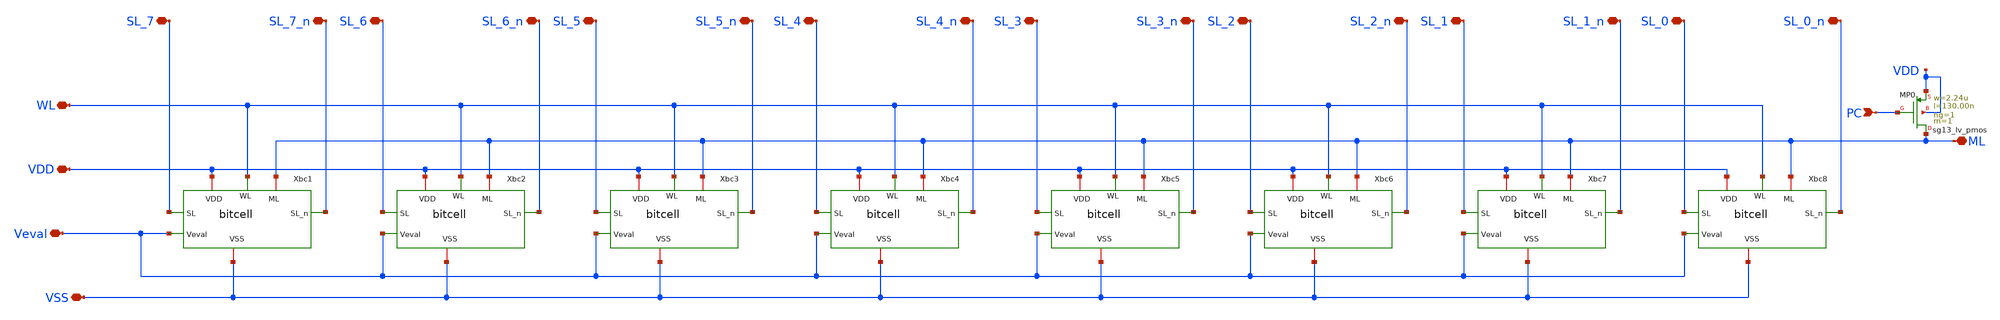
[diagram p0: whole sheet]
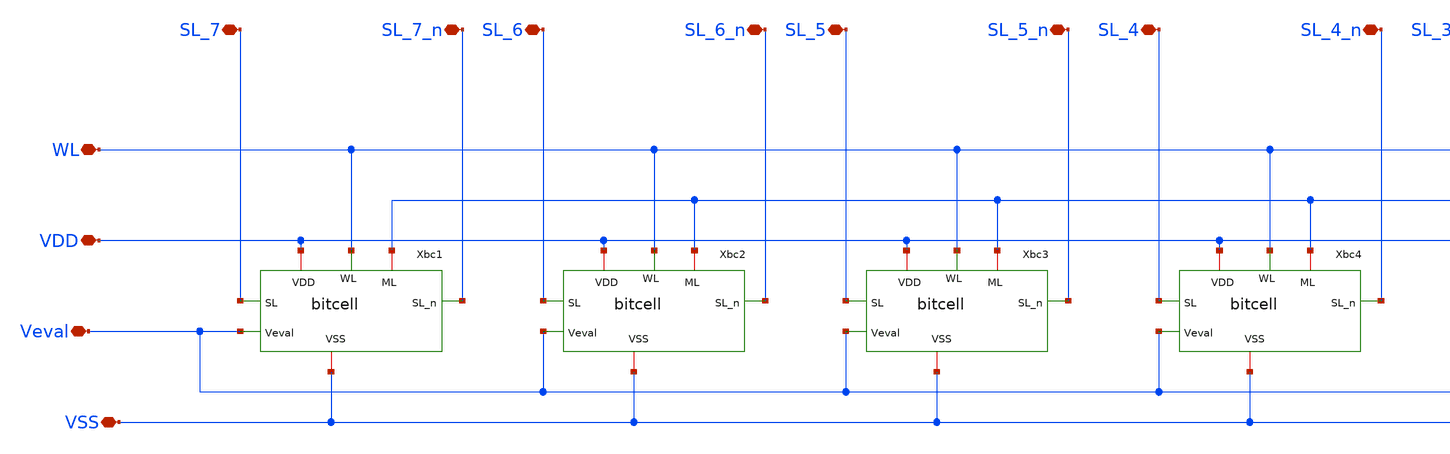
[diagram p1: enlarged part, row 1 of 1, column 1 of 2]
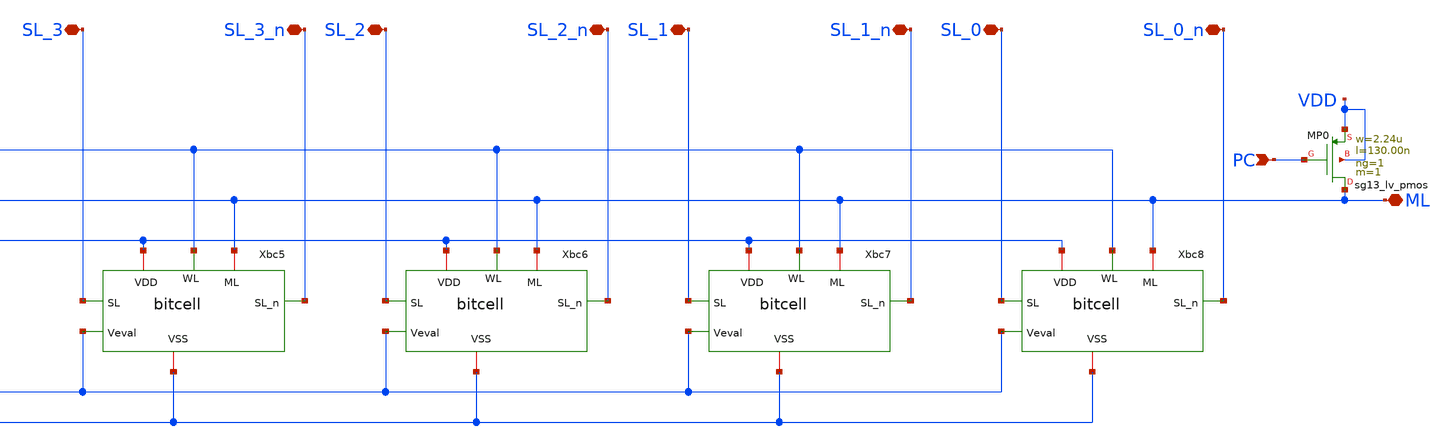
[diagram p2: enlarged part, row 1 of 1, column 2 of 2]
** sch_path: xschem/word_cell_8.sch
**.subckt word_cell_8 VSS Veval VDD WL ML SL_7 SL_6 SL_5 SL_4 SL_3 SL_2 SL_1 SL_0 SL_7_n SL_6_n
*+ SL_5_n SL_4_n SL_3_n SL_2_n SL_1_n SL_0_n PC
*.iopin VSS
*.iopin Veval
*.iopin VDD
*.iopin WL
*.iopin ML
*.iopin SL_7
*.iopin SL_6
*.iopin SL_5
*.iopin SL_4
*.iopin SL_3
*.iopin SL_2
*.iopin SL_1
*.iopin SL_0
*.iopin SL_7_n
*.iopin SL_6_n
*.iopin SL_5_n
*.iopin SL_4_n
*.iopin SL_3_n
*.iopin SL_2_n
*.iopin SL_1_n
*.iopin SL_0_n
*.ipin PC
Xbc1 WL SL_7 SL_7_n VDD ML Veval VSS bitcell
Xbc2 WL SL_6 SL_6_n VDD ML Veval VSS bitcell
Xbc3 WL SL_5 SL_5_n VDD ML Veval VSS bitcell
Xbc4 WL SL_4 SL_4_n VDD ML Veval VSS bitcell
Xbc5 WL SL_3 SL_3_n VDD ML Veval VSS bitcell
Xbc6 WL SL_2 SL_2_n VDD ML Veval VSS bitcell
Xbc7 WL SL_1 SL_1_n VDD ML Veval VSS bitcell
Xbc8 WL SL_0 SL_0_n VDD ML Veval VSS bitcell
XMP0 ML PC VDD VDD sg13_lv_pmos w=2.24u l=130.00n ng=1 m=1 mm_ok=1
**.ends

* expanding   symbol:  /home/designer/shared/bitcell.sym # of pins=7
** sym_path: xschem/bitcell.sym
** sch_path: xschem/bitcell.sch
.subckt bitcell WL SL SL_n VDD ML Veval VSS
*.ipin SL
*.ipin SL_n
*.ipin WL
*.iopin ML
*.ipin Veval
*.iopin VDD
*.iopin VSS
XMN1 SL WL D_n VSS sg13_lv_nmos w=740.00n l=130.00n ng=1 m=1 mm_ok=1
XMN2 SL_n WL D VSS sg13_lv_nmos w=740.00n l=130.00n ng=1 m=1 mm_ok=1
XMN3 net1 D_n SL VSS sg13_lv_nmos w=740.00n l=130.00n ng=1 m=1 mm_ok=1
XMN4 net1 D SL_n VSS sg13_lv_nmos w=740.00n l=130.00n ng=1 m=1 mm_ok=1
XMN5 ML net1 net2 VSS sg13_lv_nmos w=740.00n l=130.00n ng=1 m=1 mm_ok=1
XMN6 net2 Veval VSS VSS sg13_lv_nmos w=740.00n l=130.00n ng=1 m=1 mm_ok=1
X1 VDD D D_n VSS my_inv
X2 VDD D_n D VSS my_inv
.ends


* expanding   symbol:  /home/designer/shared/my_inv.sym # of pins=4
** sym_path: xschem/my_inv.sym
** sch_path: xschem/my_inv.sch
.subckt my_inv VDD Y A VSS
*.opin Y
*.ipin A
*.iopin VDD
*.iopin VSS
XMN0 Y A VSS VSS sg13_lv_nmos w=740.00n l=130.00n ng=1 m=1 mm_ok=1
XMP0 Y A VDD VDD sg13_lv_pmos w=1.12u l=130.00n ng=1 m=1 mm_ok=1
.ends

.end
